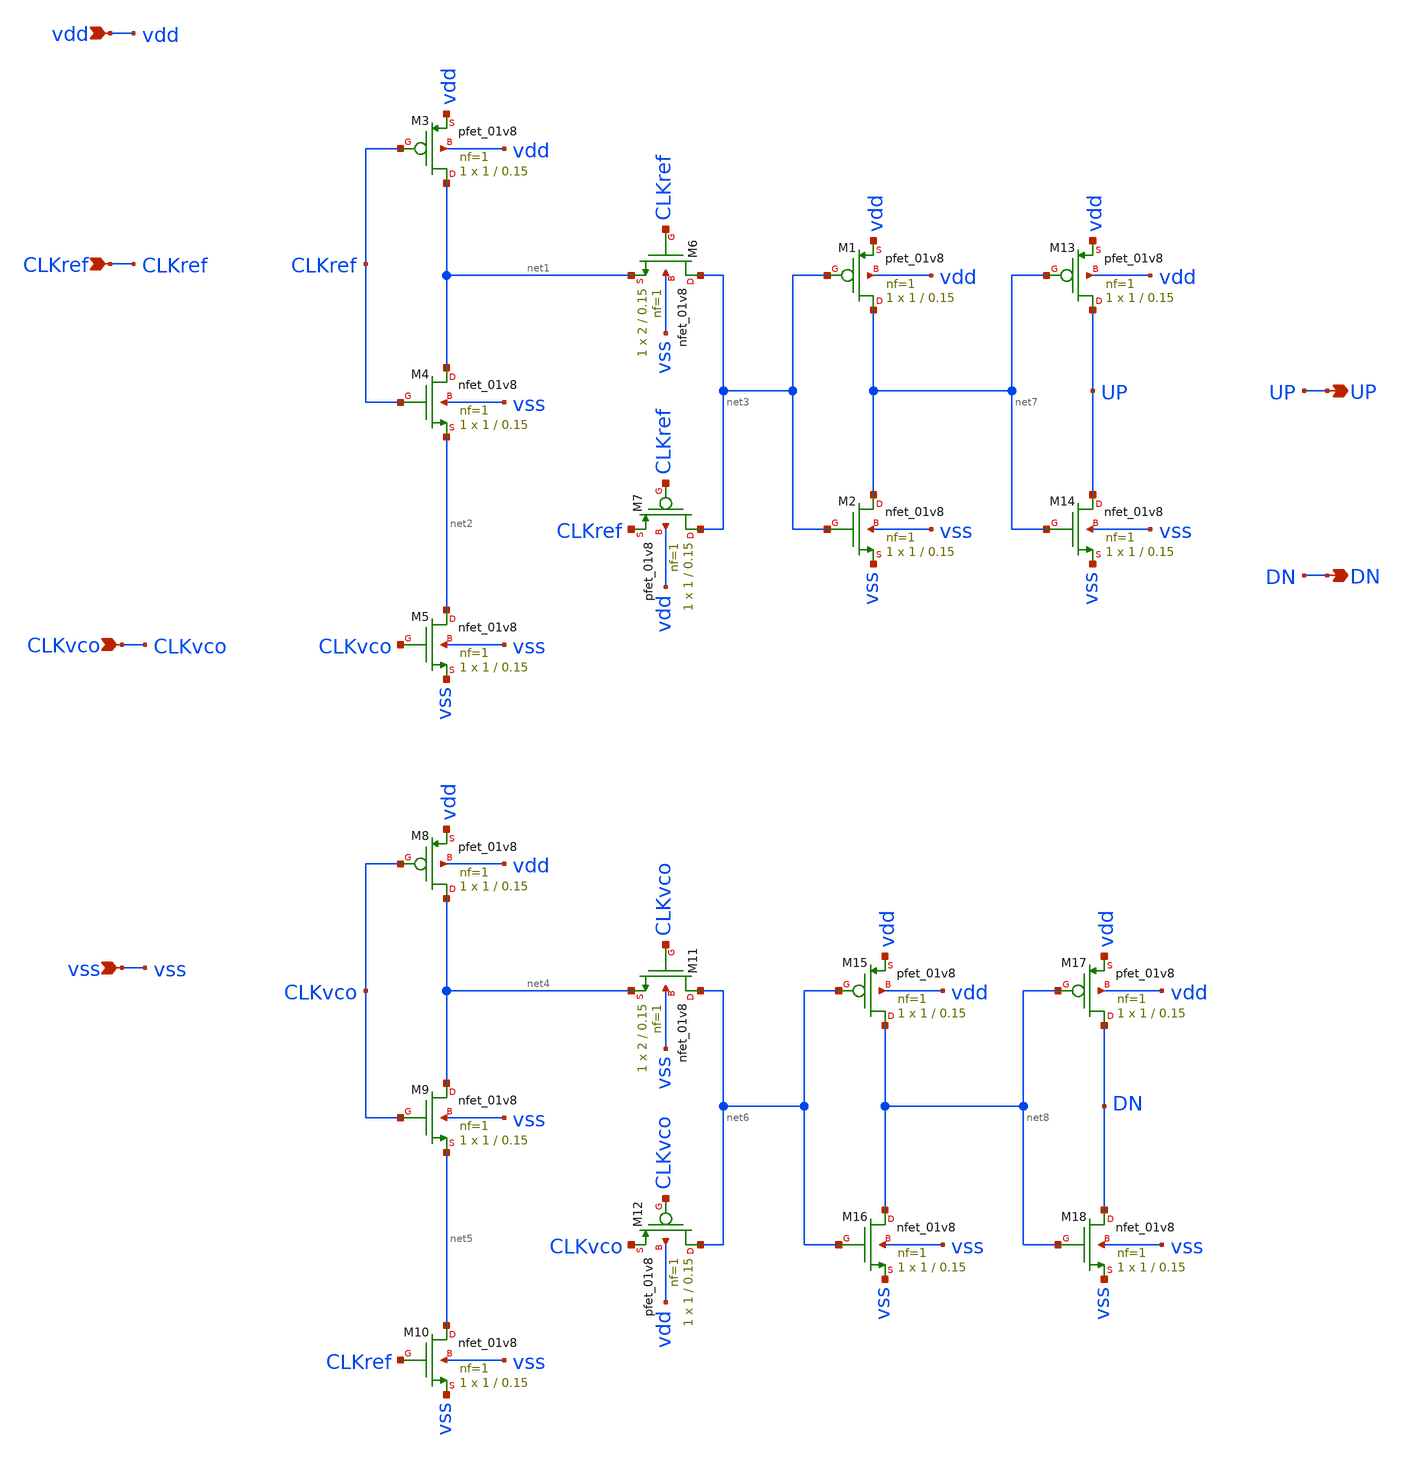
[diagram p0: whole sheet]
** sch_path: src/PFD.sch
**.subckt PFD UP CLKref CLKvco DN vdd vss
*.opin UP
*.ipin CLKref
*.ipin CLKvco
*.opin DN
*.ipin vdd
*.ipin vss
XM3 net1 CLKref vdd vdd sky130_fd_pr__pfet_01v8 L=0.15 W=1 nf=1 ad='int((1 + 1)/2) * 1 / 1 * 0.29' as='int((1 + 2)/2) * 1 / 1 * 0.29'
+ pd='2*int((1 + 1)/2) * (1 / 1 + 0.29)' ps='2*int((1 + 2)/2) * (1 / 1 + 0.29)' nrd='0.29 / 1 ' nrs='0.29 / 1 '
+ sa=0 sb=0 sd=0 mult=1 m=1
XM4 net1 CLKref net2 vss sky130_fd_pr__nfet_01v8 L=0.15 W=1 nf=1 ad='int((1 + 1)/2) * 1 / 1 * 0.29' as='int((1 + 2)/2) * 1 / 1 * 0.29'
+ pd='2*int((1 + 1)/2) * (1 / 1 + 0.29)' ps='2*int((1 + 2)/2) * (1 / 1 + 0.29)' nrd='0.29 / 1 ' nrs='0.29 / 1 '
+ sa=0 sb=0 sd=0 mult=1 m=1
XM5 net2 CLKvco vss vss sky130_fd_pr__nfet_01v8 L=0.15 W=1 nf=1 ad='int((1 + 1)/2) * 1 / 1 * 0.29' as='int((1 + 2)/2) * 1 / 1 * 0.29'
+ pd='2*int((1 + 1)/2) * (1 / 1 + 0.29)' ps='2*int((1 + 2)/2) * (1 / 1 + 0.29)' nrd='0.29 / 1 ' nrs='0.29 / 1 '
+ sa=0 sb=0 sd=0 mult=1 m=1
XM6 net3 CLKref net1 vss sky130_fd_pr__nfet_01v8 L=0.15 W=2 nf=1 ad='int((1 + 1)/2) * 2 / 1 * 0.29' as='int((1 + 2)/2) * 2 / 1 * 0.29'
+ pd='2*int((1 + 1)/2) * (2 / 1 + 0.29)' ps='2*int((1 + 2)/2) * (2 / 1 + 0.29)' nrd='0.29 / 2 ' nrs='0.29 / 2 '
+ sa=0 sb=0 sd=0 mult=1 m=1
XM7 net3 CLKref CLKref vdd sky130_fd_pr__pfet_01v8 L=0.15 W=1 nf=1 ad='int((1 + 1)/2) * 1 / 1 * 0.29'
+ as='int((1 + 2)/2) * 1 / 1 * 0.29' pd='2*int((1 + 1)/2) * (1 / 1 + 0.29)' ps='2*int((1 + 2)/2) * (1 / 1 + 0.29)'
+ nrd='0.29 / 1 ' nrs='0.29 / 1 ' sa=0 sb=0 sd=0 mult=1 m=1
XM8 net4 CLKvco vdd vdd sky130_fd_pr__pfet_01v8 L=0.15 W=1 nf=1 ad='int((1 + 1)/2) * 1 / 1 * 0.29' as='int((1 + 2)/2) * 1 / 1 * 0.29'
+ pd='2*int((1 + 1)/2) * (1 / 1 + 0.29)' ps='2*int((1 + 2)/2) * (1 / 1 + 0.29)' nrd='0.29 / 1 ' nrs='0.29 / 1 '
+ sa=0 sb=0 sd=0 mult=1 m=1
XM9 net4 CLKvco net5 vss sky130_fd_pr__nfet_01v8 L=0.15 W=1 nf=1 ad='int((1 + 1)/2) * 1 / 1 * 0.29' as='int((1 + 2)/2) * 1 / 1 * 0.29'
+ pd='2*int((1 + 1)/2) * (1 / 1 + 0.29)' ps='2*int((1 + 2)/2) * (1 / 1 + 0.29)' nrd='0.29 / 1 ' nrs='0.29 / 1 '
+ sa=0 sb=0 sd=0 mult=1 m=1
XM10 net5 CLKref vss vss sky130_fd_pr__nfet_01v8 L=0.15 W=1 nf=1 ad='int((1 + 1)/2) * 1 / 1 * 0.29' as='int((1 + 2)/2) * 1 / 1 * 0.29'
+ pd='2*int((1 + 1)/2) * (1 / 1 + 0.29)' ps='2*int((1 + 2)/2) * (1 / 1 + 0.29)' nrd='0.29 / 1 ' nrs='0.29 / 1 '
+ sa=0 sb=0 sd=0 mult=1 m=1
XM11 net6 CLKvco net4 vss sky130_fd_pr__nfet_01v8 L=0.15 W=2 nf=1 ad='int((1 + 1)/2) * 2 / 1 * 0.29'
+ as='int((1 + 2)/2) * 2 / 1 * 0.29' pd='2*int((1 + 1)/2) * (2 / 1 + 0.29)' ps='2*int((1 + 2)/2) * (2 / 1 + 0.29)'
+ nrd='0.29 / 2 ' nrs='0.29 / 2 ' sa=0 sb=0 sd=0 mult=1 m=1
XM12 net6 CLKvco CLKvco vdd sky130_fd_pr__pfet_01v8 L=0.15 W=1 nf=1 ad='int((1 + 1)/2) * 1 / 1 * 0.29'
+ as='int((1 + 2)/2) * 1 / 1 * 0.29' pd='2*int((1 + 1)/2) * (1 / 1 + 0.29)' ps='2*int((1 + 2)/2) * (1 / 1 + 0.29)'
+ nrd='0.29 / 1 ' nrs='0.29 / 1 ' sa=0 sb=0 sd=0 mult=1 m=1
XM1 net7 net3 vdd vdd sky130_fd_pr__pfet_01v8 L=0.15 W=1 nf=1 ad='int((1 + 1)/2) * 1 / 1 * 0.29' as='int((1 + 2)/2) * 1 / 1 * 0.29'
+ pd='2*int((1 + 1)/2) * (1 / 1 + 0.29)' ps='2*int((1 + 2)/2) * (1 / 1 + 0.29)' nrd='0.29 / 1 ' nrs='0.29 / 1 '
+ sa=0 sb=0 sd=0 mult=1 m=1
XM2 net7 net3 vss vss sky130_fd_pr__nfet_01v8 L=0.15 W=1 nf=1 ad='int((1 + 1)/2) * 1 / 1 * 0.29' as='int((1 + 2)/2) * 1 / 1 * 0.29'
+ pd='2*int((1 + 1)/2) * (1 / 1 + 0.29)' ps='2*int((1 + 2)/2) * (1 / 1 + 0.29)' nrd='0.29 / 1 ' nrs='0.29 / 1 '
+ sa=0 sb=0 sd=0 mult=1 m=1
XM13 UP net7 vdd vdd sky130_fd_pr__pfet_01v8 L=0.15 W=1 nf=1 ad='int((1 + 1)/2) * 1 / 1 * 0.29' as='int((1 + 2)/2) * 1 / 1 * 0.29'
+ pd='2*int((1 + 1)/2) * (1 / 1 + 0.29)' ps='2*int((1 + 2)/2) * (1 / 1 + 0.29)' nrd='0.29 / 1 ' nrs='0.29 / 1 '
+ sa=0 sb=0 sd=0 mult=1 m=1
XM14 UP net7 vss vss sky130_fd_pr__nfet_01v8 L=0.15 W=1 nf=1 ad='int((1 + 1)/2) * 1 / 1 * 0.29' as='int((1 + 2)/2) * 1 / 1 * 0.29'
+ pd='2*int((1 + 1)/2) * (1 / 1 + 0.29)' ps='2*int((1 + 2)/2) * (1 / 1 + 0.29)' nrd='0.29 / 1 ' nrs='0.29 / 1 '
+ sa=0 sb=0 sd=0 mult=1 m=1
XM15 net8 net6 vdd vdd sky130_fd_pr__pfet_01v8 L=0.15 W=1 nf=1 ad='int((1 + 1)/2) * 1 / 1 * 0.29' as='int((1 + 2)/2) * 1 / 1 * 0.29'
+ pd='2*int((1 + 1)/2) * (1 / 1 + 0.29)' ps='2*int((1 + 2)/2) * (1 / 1 + 0.29)' nrd='0.29 / 1 ' nrs='0.29 / 1 '
+ sa=0 sb=0 sd=0 mult=1 m=1
XM16 net8 net6 vss vss sky130_fd_pr__nfet_01v8 L=0.15 W=1 nf=1 ad='int((1 + 1)/2) * 1 / 1 * 0.29' as='int((1 + 2)/2) * 1 / 1 * 0.29'
+ pd='2*int((1 + 1)/2) * (1 / 1 + 0.29)' ps='2*int((1 + 2)/2) * (1 / 1 + 0.29)' nrd='0.29 / 1 ' nrs='0.29 / 1 '
+ sa=0 sb=0 sd=0 mult=1 m=1
XM17 DN net8 vdd vdd sky130_fd_pr__pfet_01v8 L=0.15 W=1 nf=1 ad='int((1 + 1)/2) * 1 / 1 * 0.29' as='int((1 + 2)/2) * 1 / 1 * 0.29'
+ pd='2*int((1 + 1)/2) * (1 / 1 + 0.29)' ps='2*int((1 + 2)/2) * (1 / 1 + 0.29)' nrd='0.29 / 1 ' nrs='0.29 / 1 '
+ sa=0 sb=0 sd=0 mult=1 m=1
XM18 DN net8 vss vss sky130_fd_pr__nfet_01v8 L=0.15 W=1 nf=1 ad='int((1 + 1)/2) * 1 / 1 * 0.29' as='int((1 + 2)/2) * 1 / 1 * 0.29'
+ pd='2*int((1 + 1)/2) * (1 / 1 + 0.29)' ps='2*int((1 + 2)/2) * (1 / 1 + 0.29)' nrd='0.29 / 1 ' nrs='0.29 / 1 '
+ sa=0 sb=0 sd=0 mult=1 m=1
**** begin user architecture code


.option temp=27

* power supplies
VDD vdd 0 1.8
VSS vss 0 0


* reference clock (20 ns period = 50 MHz)
Vref CLKref 0 pulse(0 1.8 0 1n 1n 10n 20n)

* VCO clock (slightly different frequency, 19 ns period ~52.6 MHz)
Vvco CLKvco 0 pulse(0 1.8 0 1n 1n 9.5n 19n)

* analysis
.tran 0.1n 500n
.control
run
plot v(CLKref) v(CLKvco) v(UP)+2 v(DN)+4

.endc



** opencircuitdesign pdks install
.lib $::SKYWATER_MODELS/sky130.lib.spice tt


**** end user architecture code
**.ends
.end
